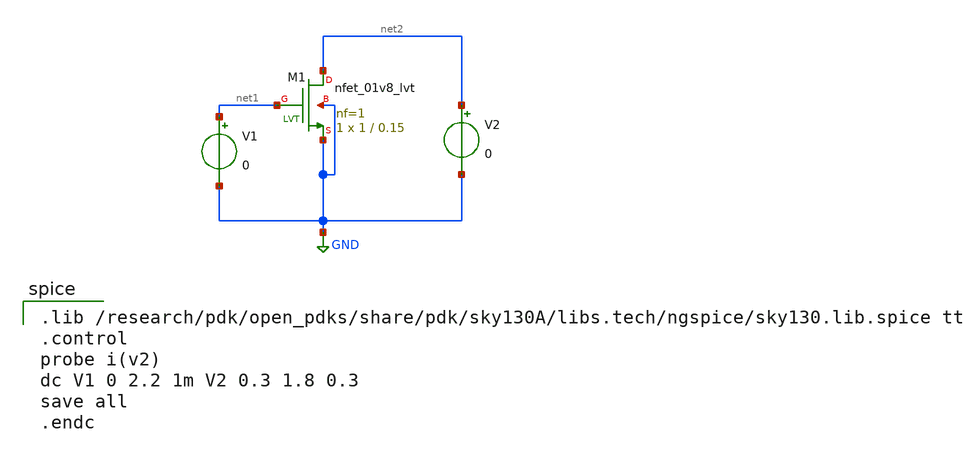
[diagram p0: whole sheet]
** sch_path: skywater_stuff/ECE631_RF_CMOS/untitled-3.sch
**.subckt untitled-3
XM1 net2 net1 GND GND sky130_fd_pr__nfet_01v8_lvt L=0.15 W=1 nf=1 ad='int((nf+1)/2) * W/nf * 0.29' as='int((nf+2)/2) * W/nf * 0.29'
+ pd='2*int((nf+1)/2) * (W/nf + 0.29)' ps='2*int((nf+2)/2) * (W/nf + 0.29)' nrd='0.29 / W' nrs='0.29 / W'
+ sa=0 sb=0 sd=0 mult=1 m=1
V1 net1 GND 0
V2 net2 GND 0
**** begin user architecture code

.lib /research/pdk/open_pdks/share/pdk/sky130A/libs.tech/ngspice/sky130.lib.spice tt
.control
probe i(v2)
dc V1 0 2.2 1m V2 0.3 1.8 0.3
save all
.endc


**** end user architecture code
**.ends
.GLOBAL GND
.end
